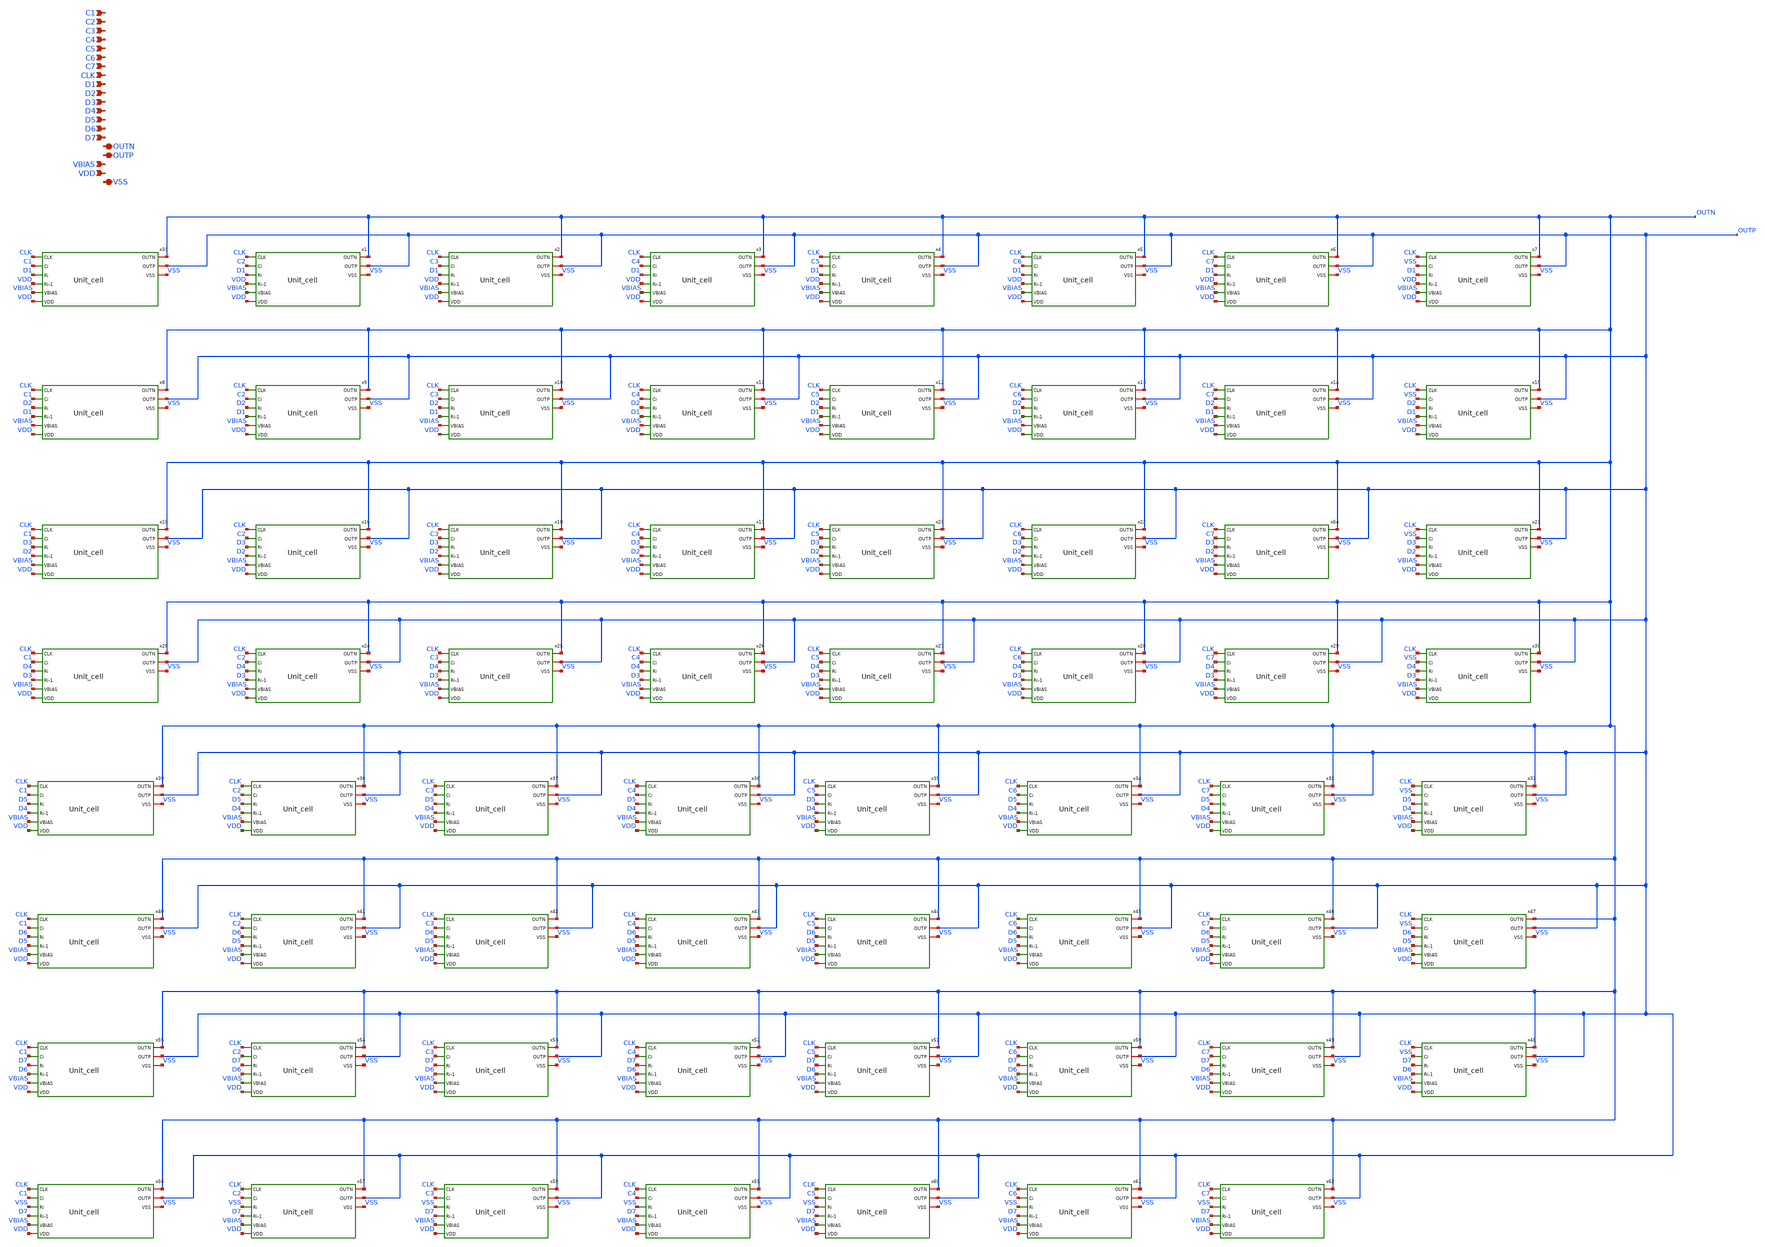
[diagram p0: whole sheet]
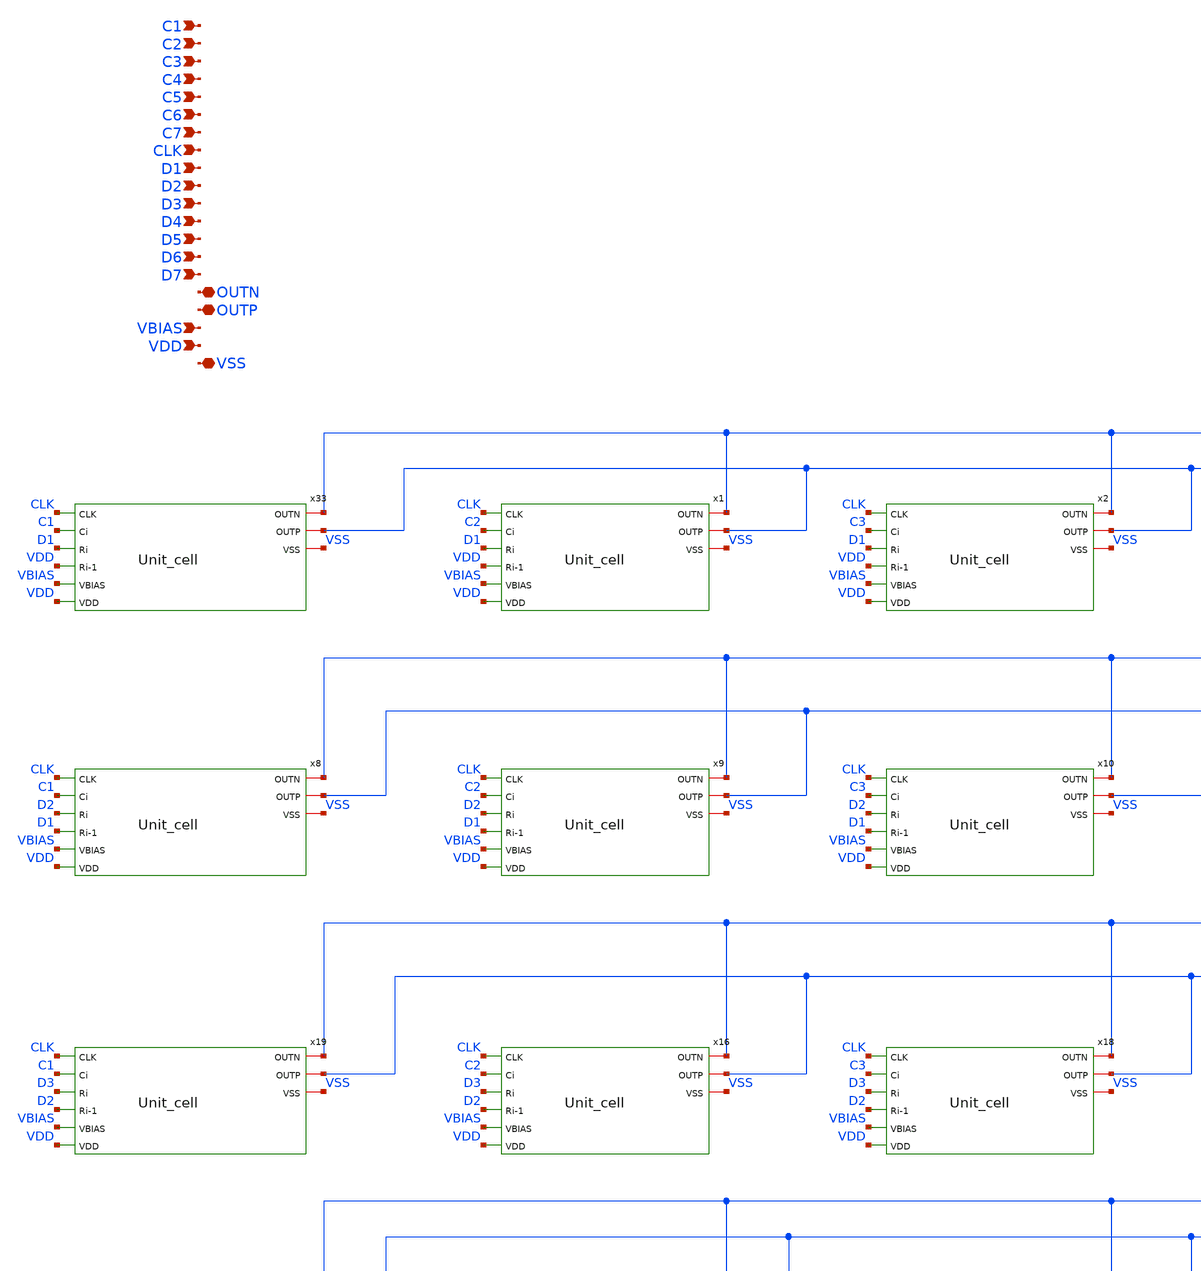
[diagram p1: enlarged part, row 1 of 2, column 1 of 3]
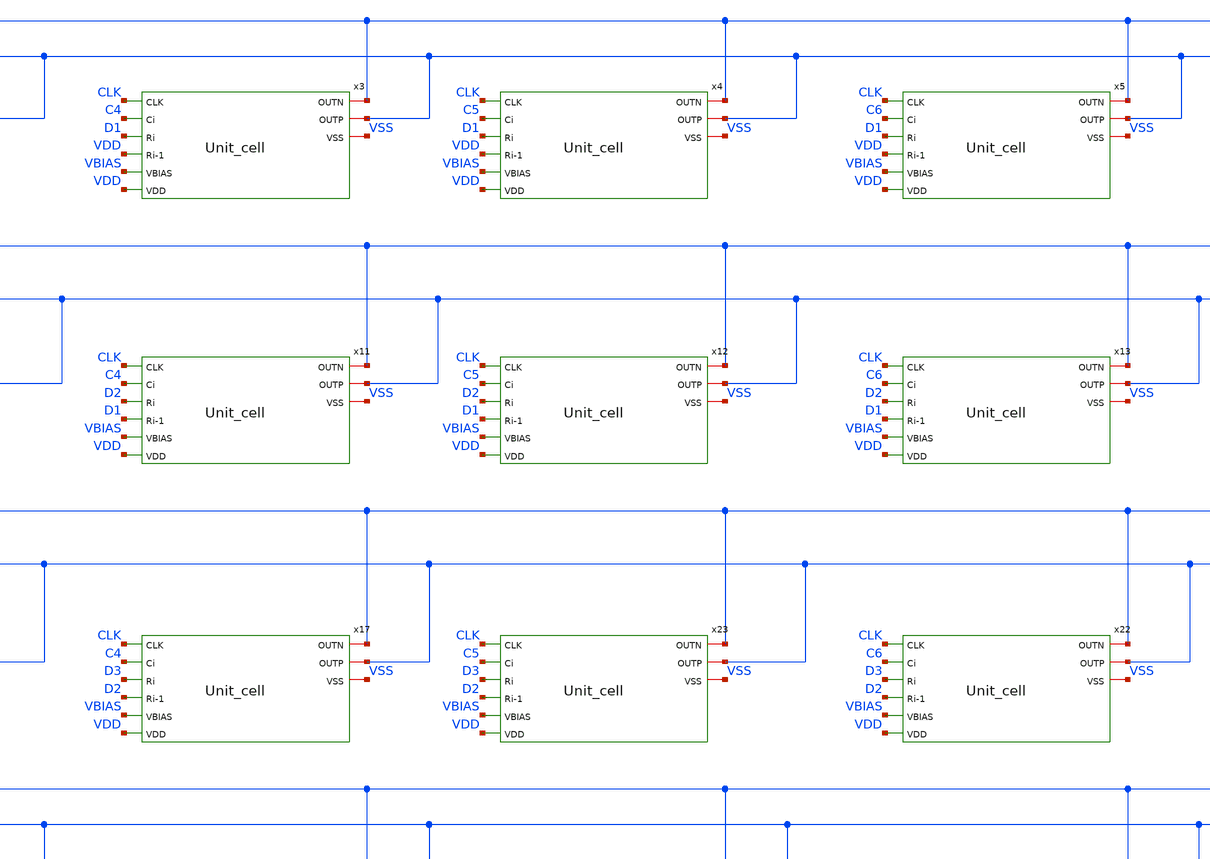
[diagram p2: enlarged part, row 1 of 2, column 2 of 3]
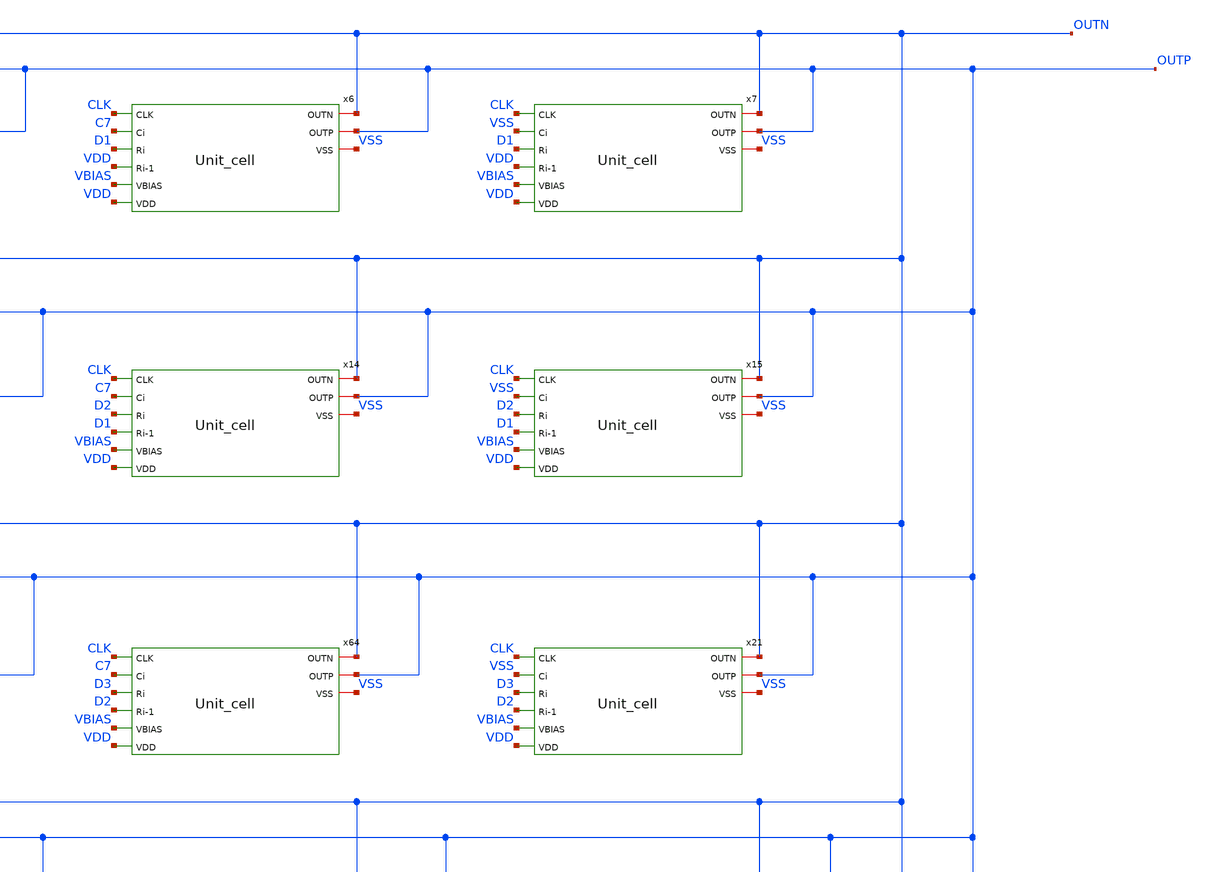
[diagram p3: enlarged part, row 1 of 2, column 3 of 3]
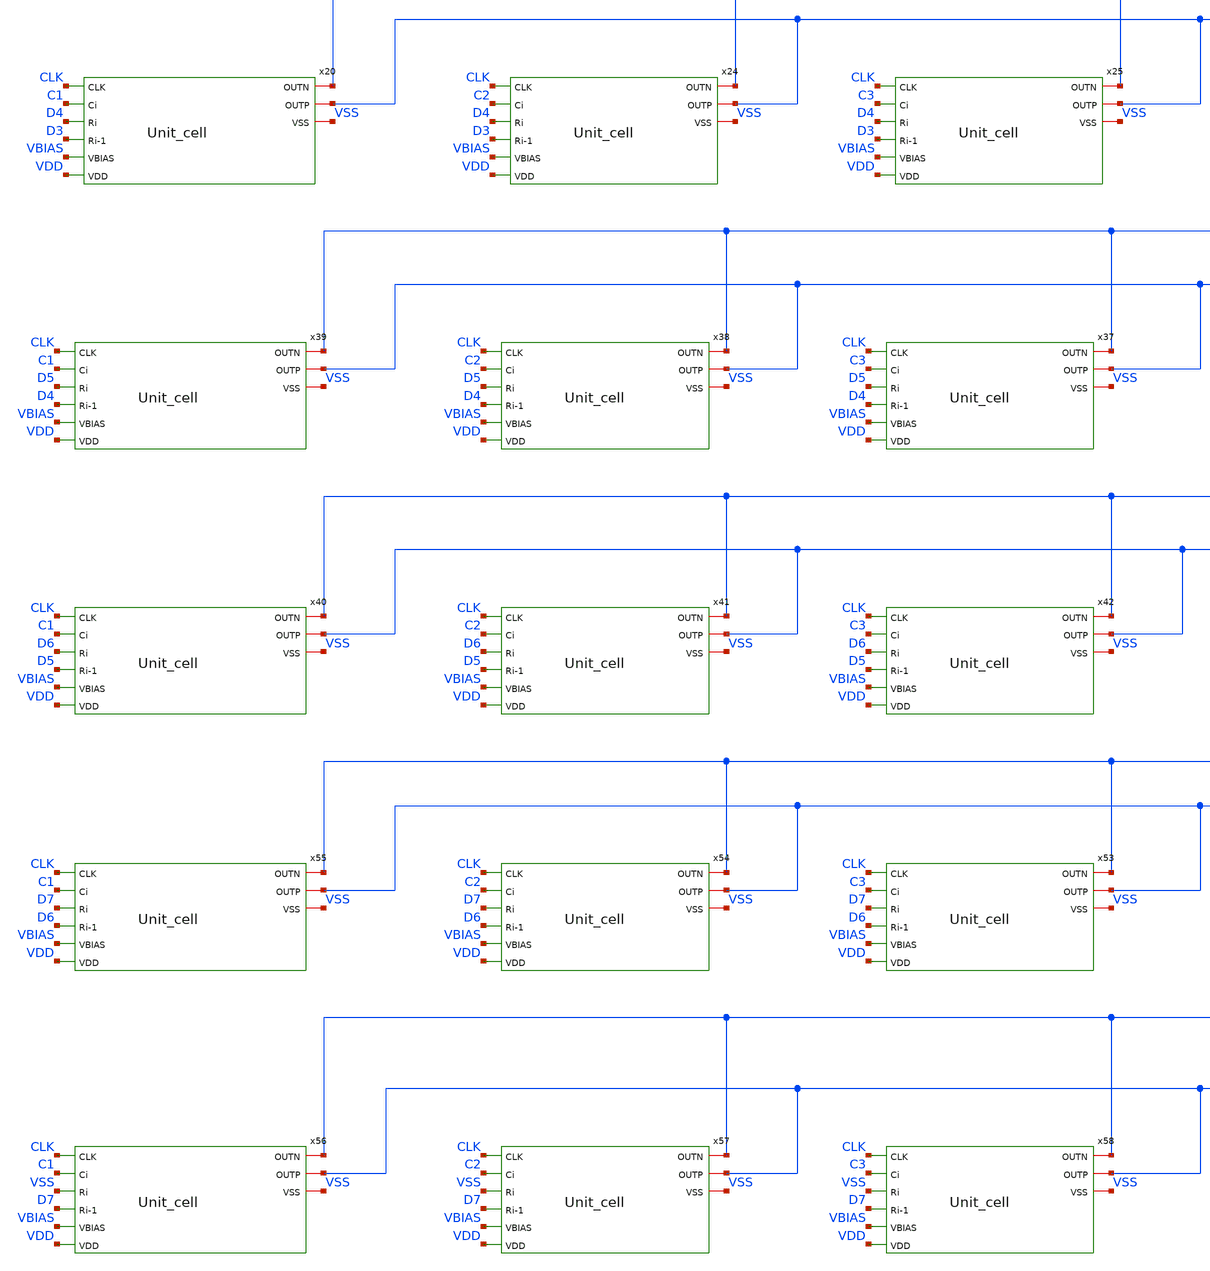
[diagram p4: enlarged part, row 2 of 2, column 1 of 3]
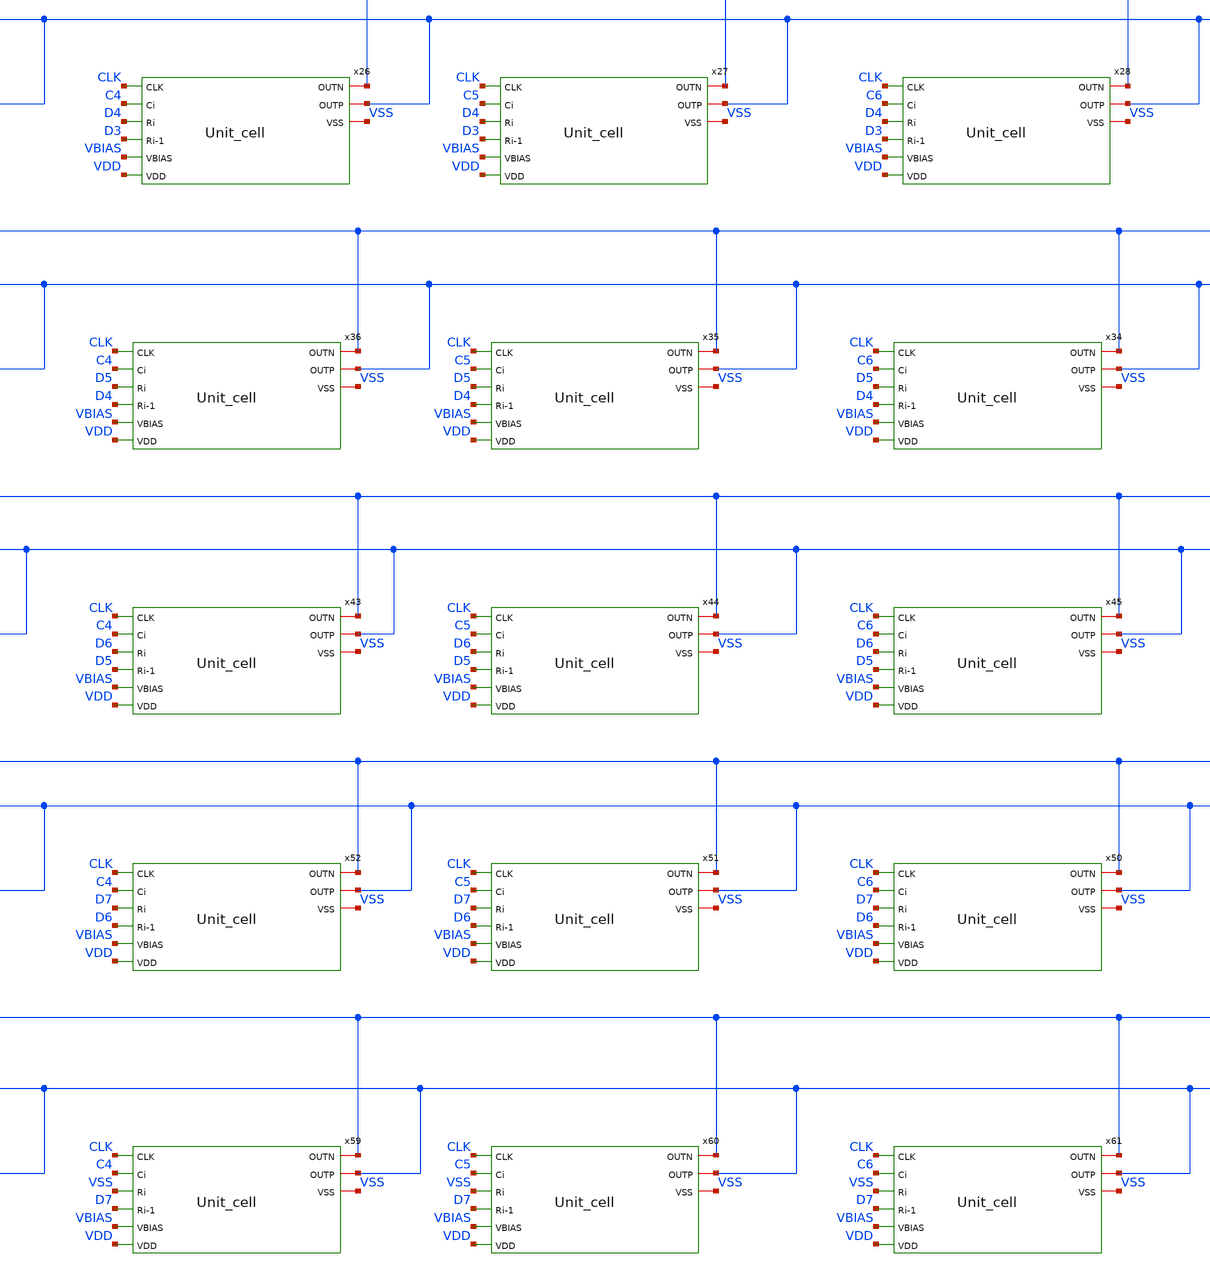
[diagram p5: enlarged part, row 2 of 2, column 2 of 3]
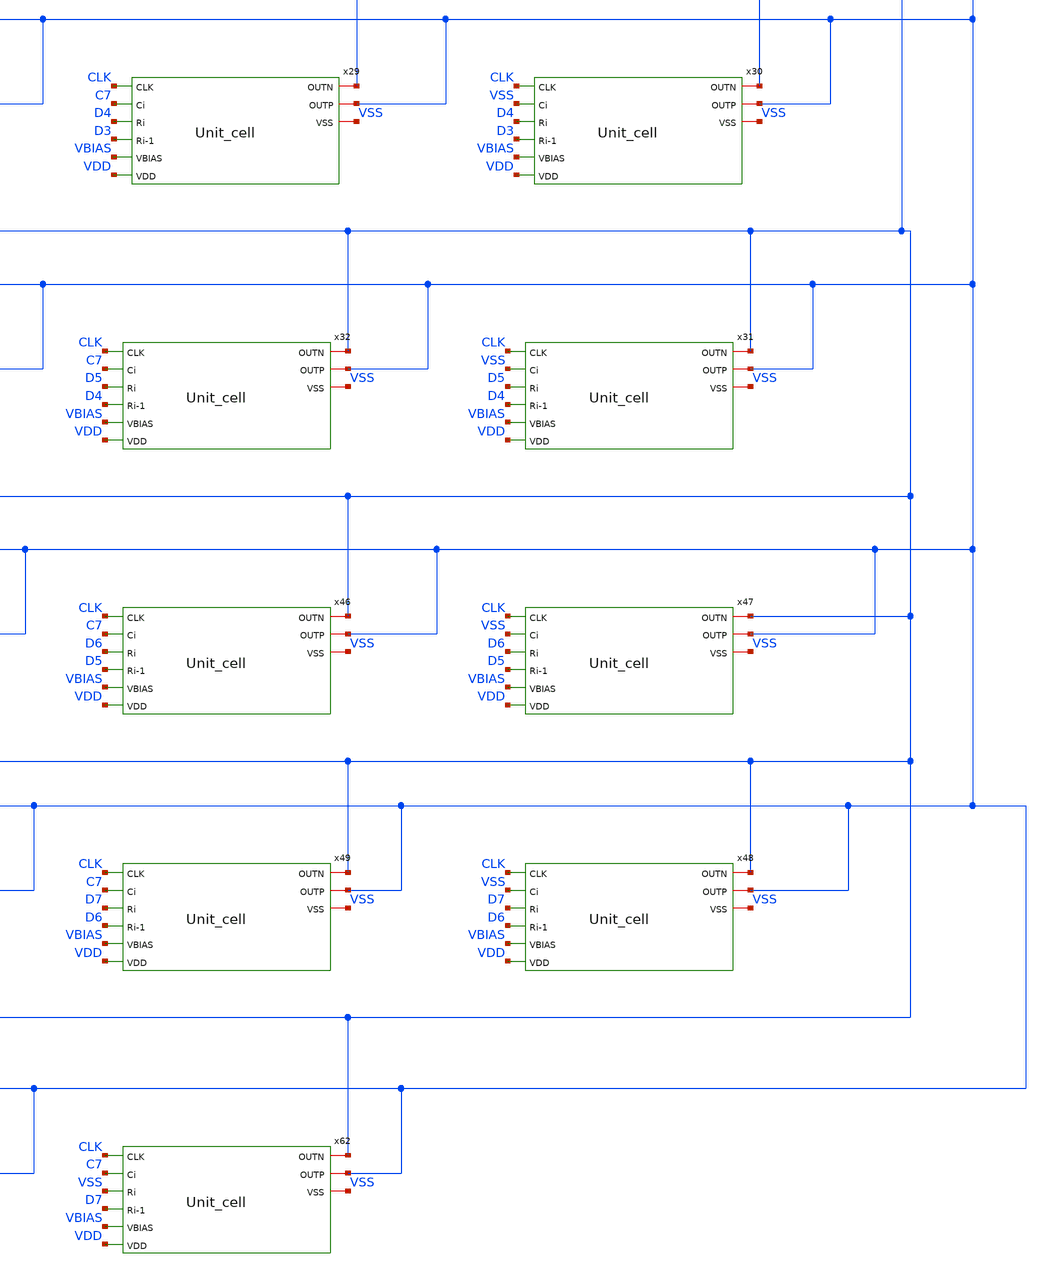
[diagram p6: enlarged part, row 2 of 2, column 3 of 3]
** sch_path: dependencies/DAC/dependencies/CS_DAC-/xschem/6MSB.sch
**.subckt 6MSB VSS VDD VBIAS OUTP OUTN D7 D6 D5 D4 D3 D2 D1 CLK C7 C6 C5 C4 C3 C2 C1
*.iopin VSS
*.ipin VDD
*.ipin VBIAS
*.iopin OUTP
*.iopin OUTN
*.ipin D7
*.ipin D6
*.ipin D5
*.ipin D4
*.ipin D3
*.ipin D2
*.ipin D1
*.ipin CLK
*.ipin C7
*.ipin C6
*.ipin C5
*.ipin C4
*.ipin C3
*.ipin C2
*.ipin C1
x33 CLK C1 OUTN OUTP D1 VDD VBIAS VDD VSS Unit_cell
x1 CLK C2 OUTN OUTP D1 VDD VBIAS VDD VSS Unit_cell
x2 CLK C3 OUTN OUTP D1 VDD VBIAS VDD VSS Unit_cell
x3 CLK C4 OUTN OUTP D1 VDD VBIAS VDD VSS Unit_cell
x4 CLK C5 OUTN OUTP D1 VDD VBIAS VDD VSS Unit_cell
x5 CLK C6 OUTN OUTP D1 VDD VBIAS VDD VSS Unit_cell
x6 CLK C7 OUTN OUTP D1 VDD VBIAS VDD VSS Unit_cell
x7 CLK VSS OUTN OUTP D1 VDD VBIAS VDD VSS Unit_cell
x8 CLK C1 OUTN OUTP D2 D1 VBIAS VDD VSS Unit_cell
x9 CLK C2 OUTN OUTP D2 D1 VBIAS VDD VSS Unit_cell
x10 CLK C3 OUTN OUTP D2 D1 VBIAS VDD VSS Unit_cell
x11 CLK C4 OUTN OUTP D2 D1 VBIAS VDD VSS Unit_cell
x12 CLK C5 OUTN OUTP D2 D1 VBIAS VDD VSS Unit_cell
x13 CLK C6 OUTN OUTP D2 D1 VBIAS VDD VSS Unit_cell
x14 CLK C7 OUTN OUTP D2 D1 VBIAS VDD VSS Unit_cell
x15 CLK VSS OUTN OUTP D2 D1 VBIAS VDD VSS Unit_cell
x64 CLK C7 OUTN OUTP D3 D2 VBIAS VDD VSS Unit_cell
x21 CLK VSS OUTN OUTP D3 D2 VBIAS VDD VSS Unit_cell
x22 CLK C6 OUTN OUTP D3 D2 VBIAS VDD VSS Unit_cell
x23 CLK C5 OUTN OUTP D3 D2 VBIAS VDD VSS Unit_cell
x17 CLK C4 OUTN OUTP D3 D2 VBIAS VDD VSS Unit_cell
x18 CLK C3 OUTN OUTP D3 D2 VBIAS VDD VSS Unit_cell
x16 CLK C2 OUTN OUTP D3 D2 VBIAS VDD VSS Unit_cell
x19 CLK C1 OUTN OUTP D3 D2 VBIAS VDD VSS Unit_cell
x20 CLK C1 OUTN OUTP D4 D3 VBIAS VDD VSS Unit_cell
x24 CLK C2 OUTN OUTP D4 D3 VBIAS VDD VSS Unit_cell
x25 CLK C3 OUTN OUTP D4 D3 VBIAS VDD VSS Unit_cell
x26 CLK C4 OUTN OUTP D4 D3 VBIAS VDD VSS Unit_cell
x27 CLK C5 OUTN OUTP D4 D3 VBIAS VDD VSS Unit_cell
x28 CLK C6 OUTN OUTP D4 D3 VBIAS VDD VSS Unit_cell
x29 CLK C7 OUTN OUTP D4 D3 VBIAS VDD VSS Unit_cell
x30 CLK VSS OUTN OUTP D4 D3 VBIAS VDD VSS Unit_cell
x31 CLK VSS OUTN OUTP D5 D4 VBIAS VDD VSS Unit_cell
x32 CLK C7 OUTN OUTP D5 D4 VBIAS VDD VSS Unit_cell
x34 CLK C6 OUTN OUTP D5 D4 VBIAS VDD VSS Unit_cell
x35 CLK C5 OUTN OUTP D5 D4 VBIAS VDD VSS Unit_cell
x36 CLK C4 OUTN OUTP D5 D4 VBIAS VDD VSS Unit_cell
x37 CLK C3 OUTN OUTP D5 D4 VBIAS VDD VSS Unit_cell
x38 CLK C2 OUTN OUTP D5 D4 VBIAS VDD VSS Unit_cell
x39 CLK C1 OUTN OUTP D5 D4 VBIAS VDD VSS Unit_cell
x40 CLK C1 OUTN OUTP D6 D5 VBIAS VDD VSS Unit_cell
x41 CLK C2 OUTN OUTP D6 D5 VBIAS VDD VSS Unit_cell
x42 CLK C3 OUTN OUTP D6 D5 VBIAS VDD VSS Unit_cell
x43 CLK C4 OUTN OUTP D6 D5 VBIAS VDD VSS Unit_cell
x44 CLK C5 OUTN OUTP D6 D5 VBIAS VDD VSS Unit_cell
x45 CLK C6 OUTN OUTP D6 D5 VBIAS VDD VSS Unit_cell
x46 CLK C7 OUTN OUTP D6 D5 VBIAS VDD VSS Unit_cell
x47 CLK VSS OUTN OUTP D6 D5 VBIAS VDD VSS Unit_cell
x48 CLK VSS OUTN OUTP D7 D6 VBIAS VDD VSS Unit_cell
x49 CLK C7 OUTN OUTP D7 D6 VBIAS VDD VSS Unit_cell
x50 CLK C6 OUTN OUTP D7 D6 VBIAS VDD VSS Unit_cell
x51 CLK C5 OUTN OUTP D7 D6 VBIAS VDD VSS Unit_cell
x52 CLK C4 OUTN OUTP D7 D6 VBIAS VDD VSS Unit_cell
x53 CLK C3 OUTN OUTP D7 D6 VBIAS VDD VSS Unit_cell
x54 CLK C2 OUTN OUTP D7 D6 VBIAS VDD VSS Unit_cell
x55 CLK C1 OUTN OUTP D7 D6 VBIAS VDD VSS Unit_cell
x56 CLK C1 OUTN OUTP VSS D7 VBIAS VDD VSS Unit_cell
x57 CLK C2 OUTN OUTP VSS D7 VBIAS VDD VSS Unit_cell
x58 CLK C3 OUTN OUTP VSS D7 VBIAS VDD VSS Unit_cell
x59 CLK C4 OUTN OUTP VSS D7 VBIAS VDD VSS Unit_cell
x60 CLK C5 OUTN OUTP VSS D7 VBIAS VDD VSS Unit_cell
x61 CLK C6 OUTN OUTP VSS D7 VBIAS VDD VSS Unit_cell
x62 CLK C7 OUTN OUTP VSS D7 VBIAS VDD VSS Unit_cell
**.ends
.end
